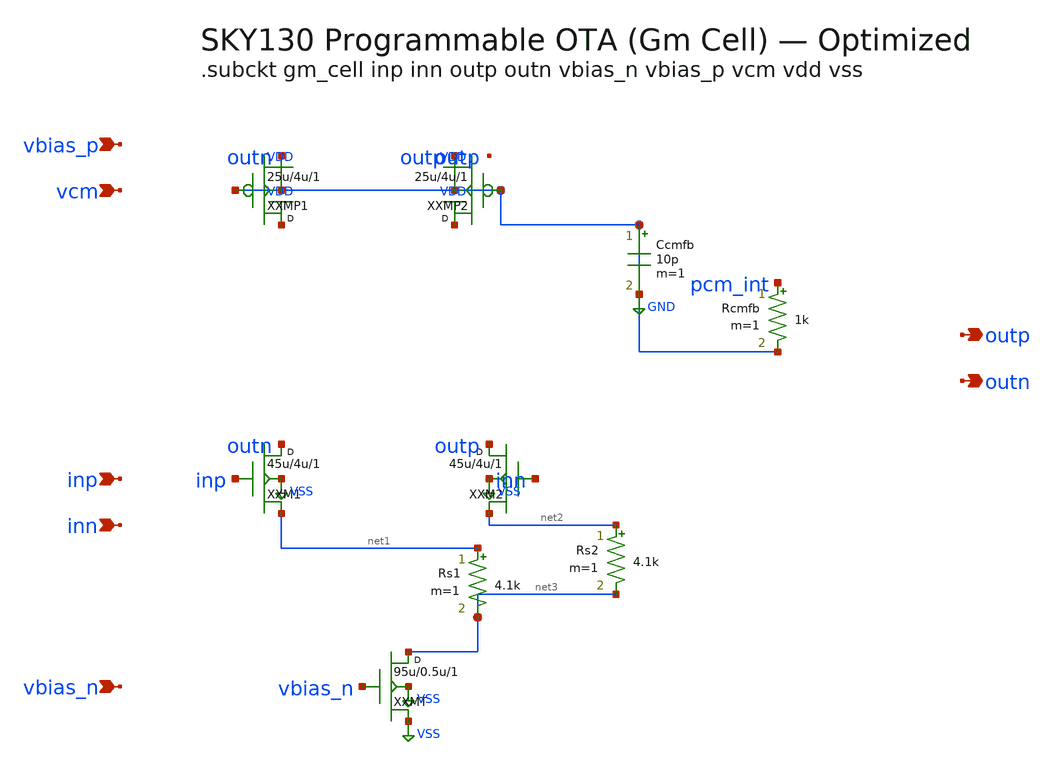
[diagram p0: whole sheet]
** sch_path: data/sch/ode_gm-cell.sch
**.subckt ode_gm-cell inp inn vbias_n vbias_p vcm outp outn
*.ipin inp
*.ipin inn
*.ipin vbias_n
*.ipin vbias_p
*.ipin vcm
*.opin outp
*.opin outn
XXM1 outn inp net1 VSS sky130_fd_pr__nfet_01v8 w=45u l=4u m=1
XXM2 outp inn net2 VSS sky130_fd_pr__nfet_01v8 w=45u l=4u m=1
Rs1 net1 net3 4.1k m=1
Rs2 net2 net3 4.1k m=1
XXMT net3 vbias_n VSS VSS sky130_fd_pr__nfet_01v8 w=95u l=0.5u m=1
XXMP1 VDD VDD outn VDD sky130_fd_pr__pfet_01v8 w=25u l=4u m=1
XXMP2 VDD VDD outp VDD sky130_fd_pr__pfet_01v8 w=25u l=4u m=1
Rcmfb pcm_int VDD 1k m=1
Ccmfb VDD VDD 10p m=1
**.ends
.GLOBAL VSS
.GLOBAL VDD
.GLOBAL GND
.end
